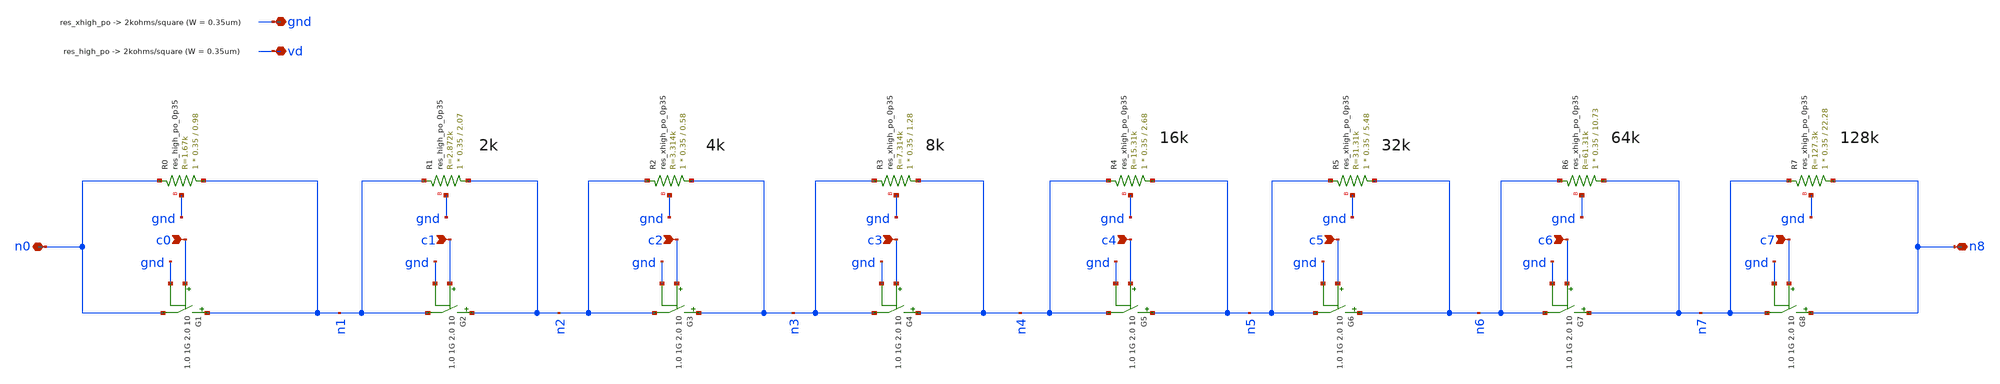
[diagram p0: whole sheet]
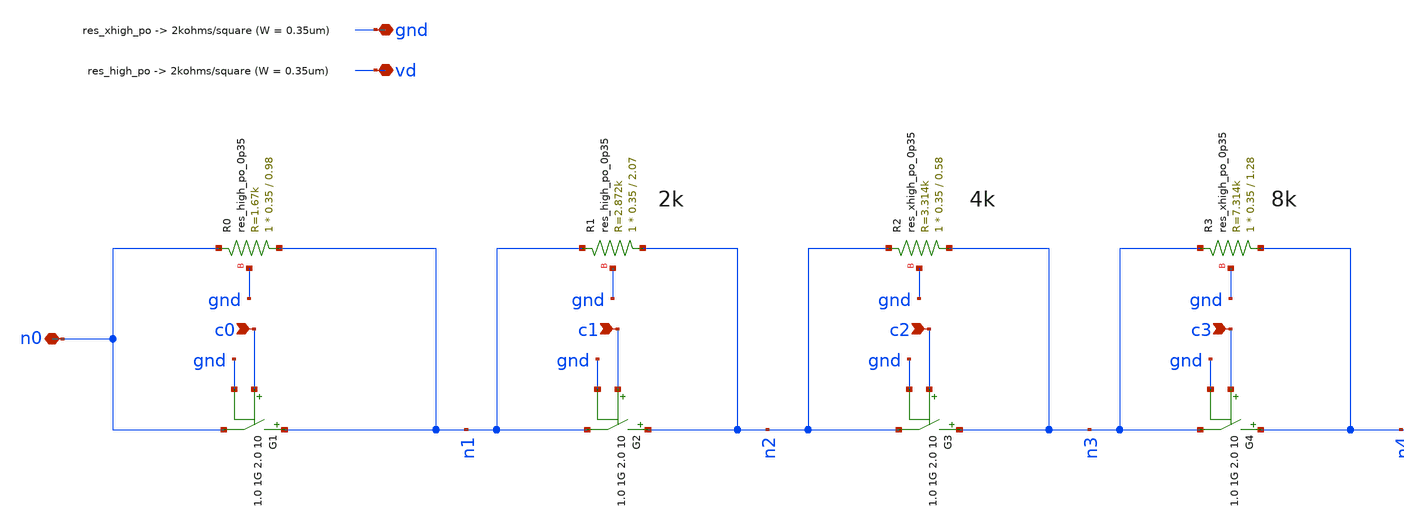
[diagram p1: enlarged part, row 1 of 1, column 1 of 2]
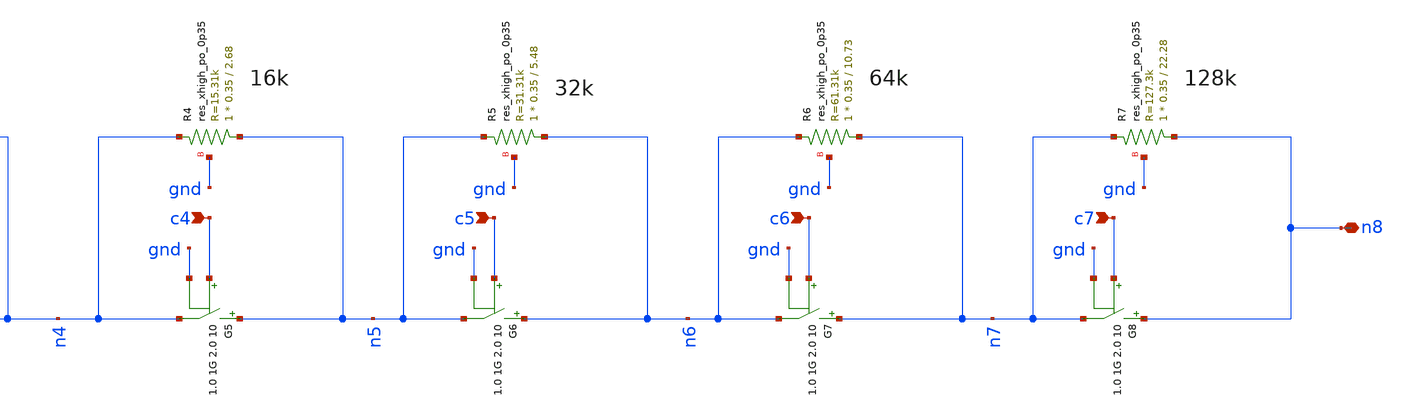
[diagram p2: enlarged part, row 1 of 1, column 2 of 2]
** sch_path: xschem/digpot.sch
**.subckt digpot c0 c1 c2 c3 c4 c5 c6 c7 gnd vd n0 n8
*.ipin c0
*.ipin c1
*.ipin c2
*.ipin c3
*.ipin c4
*.ipin c5
*.ipin c6
*.ipin c7
*.iopin gnd
*.iopin vd
*.iopin n0
*.iopin n8
XR0 n1 n0 gnd sky130_fd_pr__res_high_po_0p35 L=0.98 mult=1 m=1
XR1 n2 n1 gnd sky130_fd_pr__res_high_po_0p35 L=2.07 mult=1 m=1
XR2 n3 n2 gnd sky130_fd_pr__res_xhigh_po_0p35 L=0.58 mult=1 m=1
XR3 n4 n3 gnd sky130_fd_pr__res_xhigh_po_0p35 L=1.28 mult=1 m=1
XR4 n5 n4 gnd sky130_fd_pr__res_xhigh_po_0p35 L=2.68 mult=1 m=1
XR5 n6 n5 gnd sky130_fd_pr__res_xhigh_po_0p35 L=5.48 mult=1 m=1
XR6 n7 n6 gnd sky130_fd_pr__res_xhigh_po_0p35 L=10.73 mult=1 m=1
XR7 n8 n7 gnd sky130_fd_pr__res_xhigh_po_0p35 L=22.28 mult=1 m=1
G1 n1 n0 vcr pwl(1) c0 gnd 1.0 1G 2.0 10
G2 n2 n1 vcr pwl(1) c1 gnd 1.0 1G 2.0 10
G3 n3 n2 vcr pwl(1) c2 gnd 1.0 1G 2.0 10
G4 n4 n3 vcr pwl(1) c3 gnd 1.0 1G 2.0 10
G5 n5 n4 vcr pwl(1) c4 gnd 1.0 1G 2.0 10
G6 n6 n5 vcr pwl(1) c5 gnd 1.0 1G 2.0 10
G7 n7 n6 vcr pwl(1) c6 gnd 1.0 1G 2.0 10
G8 n8 n7 vcr pwl(1) c7 gnd 1.0 1G 2.0 10
**.ends
.end
